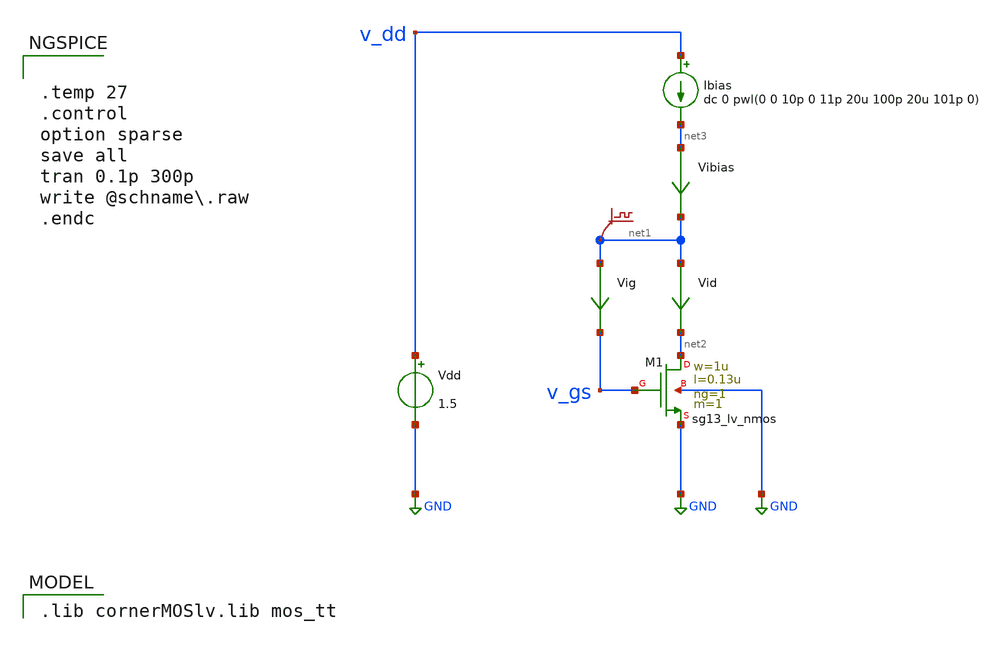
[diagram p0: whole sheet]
** sch_path: xschem/mosfet_diode_settling.sch
* (c) 2024-2025 Harald Pretl, Apache-2.0 license
**.subckt mosfet_diode_settling
Vdd v_dd GND 1.5
XM1 net2 v_gs GND GND sg13_lv_nmos w=1u l=0.13u ng=1 m=1 mm_ok=1
Ibias v_dd net3 dc 0 pwl(0 0 10p 0 11p 20u 100p 20u 101p 0)
.save v(net1)
Vid net1 net2 0
.save i(vid)
Vibias net3 net1 0
.save i(vibias)
Vig net1 v_gs 0
.save i(vig)
**** begin user architecture code
 .lib cornerMOSlv.lib mos_tt



.temp 27
.control
option sparse
save all
tran 0.1p 300p
write @schname\.raw
.endc


**** end user architecture code
**.ends
.GLOBAL GND
.end
